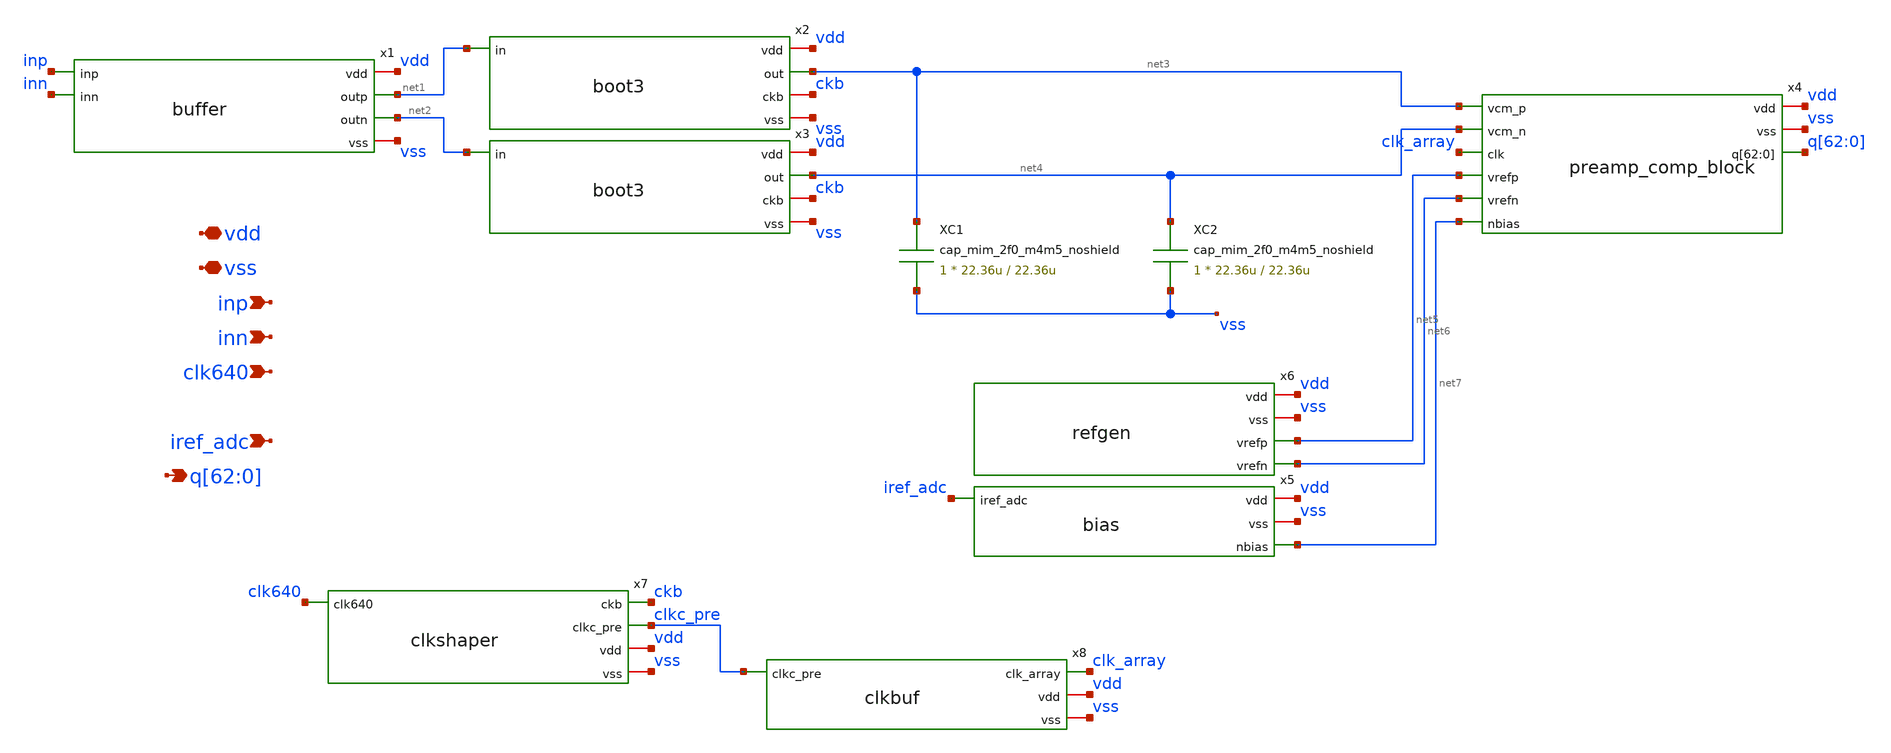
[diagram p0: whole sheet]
** sch_path: blocks/adc/comp-array/compact/block_top.sch
**.subckt block_top vdd vss inp inn clk640 iref_adc
*+ q[62],q[61],q[60],q[59],q[58],q[57],q[56],q[55],q[54],q[53],q[52],q[51],q[50],q[49],q[48],q[47],q[46],q[45],q[44],q[43],q[42],q[41],q[40],q[39],q[38],q[37],q[36],q[35],q[34],q[33],q[32],q[31],q[30],q[29],q[28],q[27],q[26],q[25],q[24],q[23],q[22],q[21],q[20],q[19],q[18],q[17],q[16],q[15],q[14],q[13],q[12],q[11],q[10],q[9],q[8],q[7],q[6],q[5],q[4],q[3],q[2],q[1],q[0]
*.iopin vdd
*.iopin vss
*.ipin inp
*.ipin inn
*.ipin clk640
*.ipin iref_adc
*.opin
*+ q[62],q[61],q[60],q[59],q[58],q[57],q[56],q[55],q[54],q[53],q[52],q[51],q[50],q[49],q[48],q[47],q[46],q[45],q[44],q[43],q[42],q[41],q[40],q[39],q[38],q[37],q[36],q[35],q[34],q[33],q[32],q[31],q[30],q[29],q[28],q[27],q[26],q[25],q[24],q[23],q[22],q[21],q[20],q[19],q[18],q[17],q[16],q[15],q[14],q[13],q[12],q[11],q[10],q[9],q[8],q[7],q[6],q[5],q[4],q[3],q[2],q[1],q[0]
x1 vdd inp inn net1 net2 vss buffer
x2 vdd net1 net3 ckb vss boot3
x3 vdd net2 net4 ckb vss boot3
XC1 net3 vss cap_mim_2f0_m4m5_noshield c_width=22.36u c_length=22.36u m=1
XC2 net4 vss cap_mim_2f0_m4m5_noshield c_width=22.36u c_length=22.36u m=1
x4 vdd vss net3 net4 clk_array q[62] q[61] q[60] q[59] q[58] q[57] q[56] q[55] q[54] q[53] q[52]
+ q[51] q[50] q[49] q[48] q[47] q[46] q[45] q[44] q[43] q[42] q[41] q[40] q[39] q[38] q[37] q[36] q[35]
+ q[34] q[33] q[32] q[31] q[30] q[29] q[28] q[27] q[26] q[25] q[24] q[23] q[22] q[21] q[20] q[19] q[18]
+ q[17] q[16] q[15] q[14] q[13] q[12] q[11] q[10] q[9] q[8] q[7] q[6] q[5] q[4] q[3] q[2] q[1] q[0] net5
+ net6 net7 preamp_comp_block
x5 vdd vss net7 iref_adc bias
x6 vdd vss net5 net6 refgen
x7 clk640 ckb clkc_pre vdd vss clkshaper
x8 clkc_pre clk_array vdd vss clkbuf
**.ends
.end
